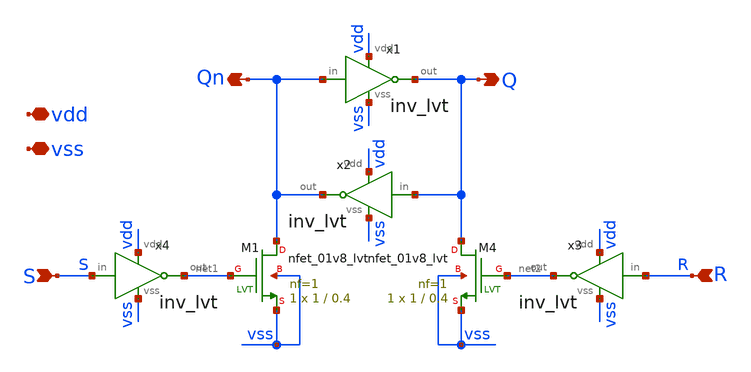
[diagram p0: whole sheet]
** sch_path: xschem/sar/latch/latch.sch
**.subckt latch S R vss vdd Q Qn
*.ipin S
*.ipin R
*.iopin vss
*.iopin vdd
*.opin Q
*.opin Qn
x1 vdd Qn Q vss inv_lvt
x2 vdd Q Qn vss inv_lvt
x3 vdd R net2 vss inv_lvt
x4 vdd S net1 vss inv_lvt
XM4 Q net2 vss vss sky130_fd_pr__nfet_01v8_lvt L=0.4 W=1 nf=1 ad='int((nf+1)/2) * W/nf * 0.29' as='int((nf+2)/2) * W/nf * 0.29'
+ pd='2*int((nf+1)/2) * (W/nf + 0.29)' ps='2*int((nf+2)/2) * (W/nf + 0.29)' nrd='0.29 / W' nrs='0.29 / W'
+ sa=0 sb=0 sd=0 mult=1 m=1
XM1 Qn net1 vss vss sky130_fd_pr__nfet_01v8_lvt L=0.4 W=1 nf=1 ad='int((nf+1)/2) * W/nf * 0.29' as='int((nf+2)/2) * W/nf * 0.29'
+ pd='2*int((nf+1)/2) * (W/nf + 0.29)' ps='2*int((nf+2)/2) * (W/nf + 0.29)' nrd='0.29 / W' nrs='0.29 / W'
+ sa=0 sb=0 sd=0 mult=1 m=1
**.ends

* expanding   symbol:  logic/inv_lvt.sym # of pins=4
** sym_path: logic/inv_lvt.sym
** sch_path: logic/inv_lvt.sch
.subckt inv_lvt vdd in out vss
*.iopin vdd
*.iopin vss
*.ipin in
*.opin out
XM3 out in vss vss sky130_fd_pr__nfet_01v8_lvt L=0.4 W=1 nf=1 ad='int((nf+1)/2) * W/nf * 0.29' as='int((nf+2)/2) * W/nf * 0.29'
+ pd='2*int((nf+1)/2) * (W/nf + 0.29)' ps='2*int((nf+2)/2) * (W/nf + 0.29)' nrd='0.29 / W' nrs='0.29 / W'
+ sa=0 sb=0 sd=0 mult=1 m=1
XM1 out in vdd vdd sky130_fd_pr__pfet_01v8_lvt L=0.4 W=1 nf=1 ad='int((nf+1)/2) * W/nf * 0.29' as='int((nf+2)/2) * W/nf * 0.29'
+ pd='2*int((nf+1)/2) * (W/nf + 0.29)' ps='2*int((nf+2)/2) * (W/nf + 0.29)' nrd='0.29 / W' nrs='0.29 / W'
+ sa=0 sb=0 sd=0 mult=1 m=1
.ends

.end
